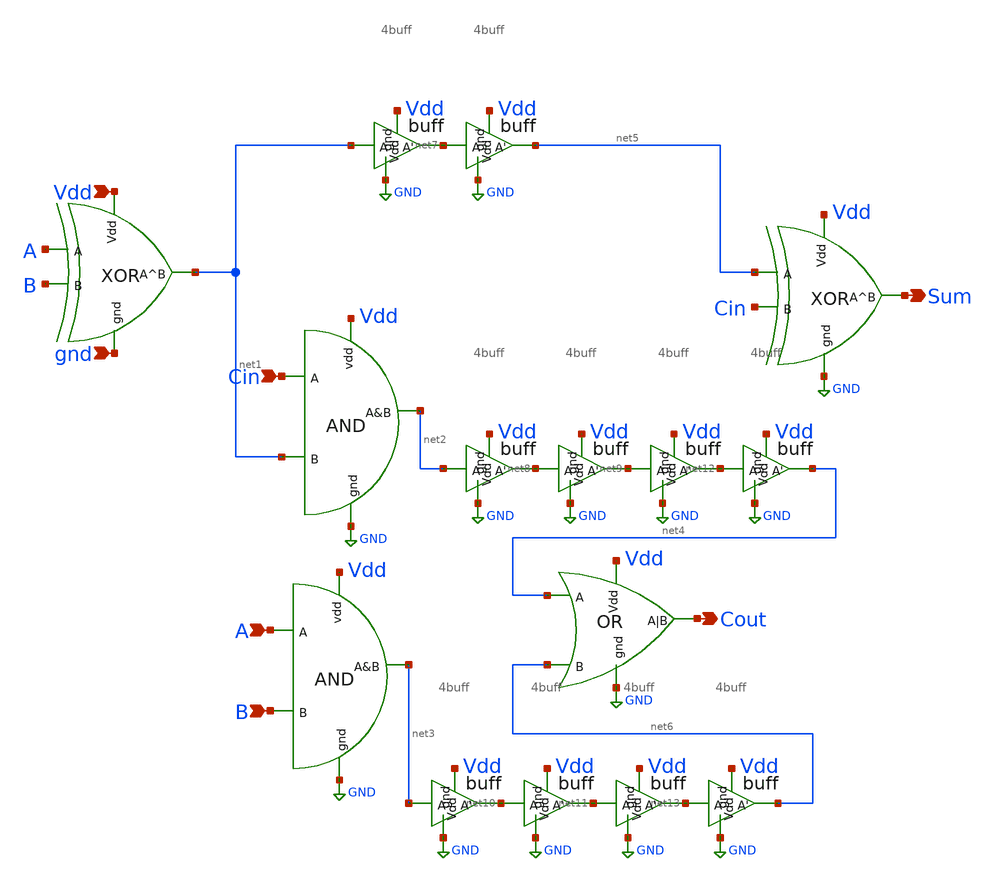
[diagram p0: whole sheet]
** sch_path: extra_stuff/full_adder.sch
**.subckt full_adder Vdd gnd A B Cin Sum Cout
*.ipin Vdd
*.ipin gnd
*.ipin A
*.ipin B
*.ipin Cin
*.opin Sum
*.opin Cout
x1 Vdd gnd net1 A B xor
x2 Vdd GND Sum net5 Cin xor
x3 Cin net1 net2 Vdd GND and
x4 A B net3 Vdd GND and
x5 Vdd GND Cout net4 net6 or
x6 net7 GND net1 Vdd 4buff
x7 net5 GND net7 Vdd 4buff
x8 net8 GND net2 Vdd 4buff
x9 net9 GND net8 Vdd 4buff
x10 net10 GND net3 Vdd 4buff
x11 net11 GND net10 Vdd 4buff
x14 net12 GND net9 Vdd 4buff
x15 net4 GND net12 Vdd 4buff
x16 net13 GND net11 Vdd 4buff
x17 net6 GND net13 Vdd 4buff
**.ends
.GLOBAL GND
.end
